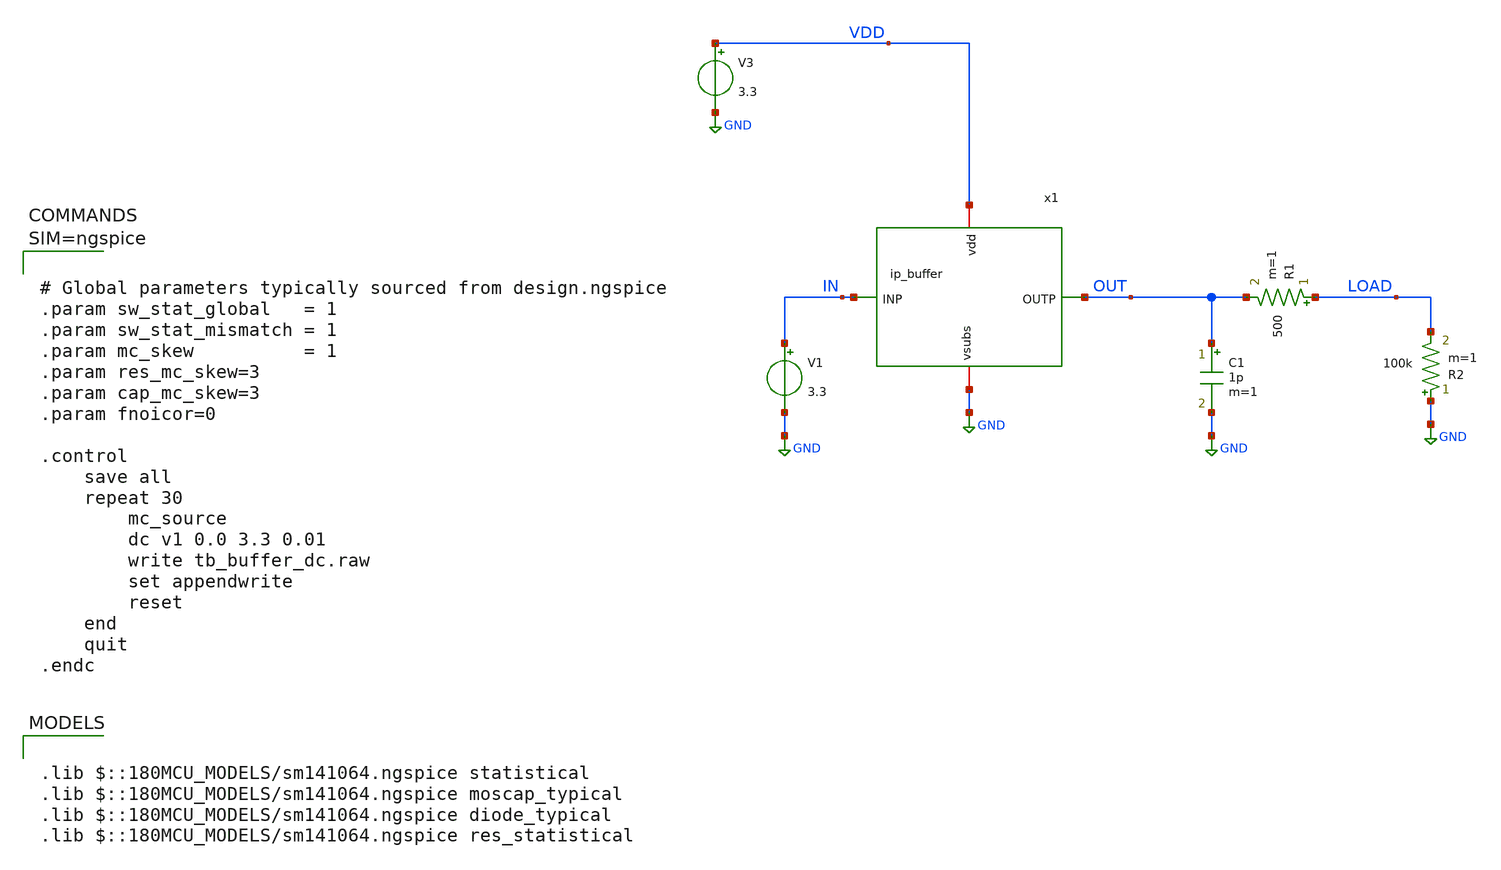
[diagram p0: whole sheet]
** sch_path: xschem/tb_buffer_dc.sch
**.subckt tb_buffer_dc
x1 VDD OUT IN GND ip_buffer
V3 VDD GND 3.3
V1 IN GND 3.3
R1 LOAD OUT 500 m=1
C1 OUT GND 1p m=1
R2 GND LOAD 100k m=1
**** begin user architecture code

.lib $::180MCU_MODELS/sm141064.ngspice statistical
.lib $::180MCU_MODELS/sm141064.ngspice moscap_typical
.lib $::180MCU_MODELS/sm141064.ngspice diode_typical
.lib $::180MCU_MODELS/sm141064.ngspice res_statistical




# Global parameters typically sourced from design.ngspice
.param sw_stat_global   = 1
.param sw_stat_mismatch = 1
.param mc_skew          = 1
.param res_mc_skew=3
.param cap_mc_skew=3
.param fnoicor=0

.control
	save all
	repeat 30
		mc_source
		dc v1 0.0 3.3 0.01
		write tb_buffer_dc.raw
		set appendwrite
		reset
	end
	quit
.endc



**** end user architecture code
**.ends

* expanding   symbol:  ip_buffer.sym # of pins=4
** sym_path: xschem/ip_buffer.sym
** sch_path: xschem/ip_buffer.sch
.subckt ip_buffer vdd OUTP INP vsubs
*.iopin vsubs
*.iopin vdd
*.ipin INP
*.opin OUTP
XM1 vsubs INP OUTP OUTP pfet_06v0 L=1u W=10u nf=1 ad='int((nf+1)/2) * W/nf * 0.18u' as='int((nf+2)/2) * W/nf * 0.18u'
+ pd='2*int((nf+1)/2) * (W/nf + 0.18u)' ps='2*int((nf+2)/2) * (W/nf + 0.18u)' nrd='0.18u / W' nrs='0.18u / W'
+ sa=0 sb=0 sd=0 m=15
Vmeas net1 net2 0
XM4 OUTP net1 vdd vdd pfet_06v0 L=2u W=10u nf=1 ad='int((nf+1)/2) * W/nf * 0.18u' as='int((nf+2)/2) * W/nf * 0.18u'
+ pd='2*int((nf+1)/2) * (W/nf + 0.18u)' ps='2*int((nf+2)/2) * (W/nf + 0.18u)' nrd='0.18u / W' nrs='0.18u / W'
+ sa=0 sb=0 sd=0 m=5
XM2 net1 net1 vdd vdd pfet_06v0 L=2u W=10u nf=1 ad='int((nf+1)/2) * W/nf * 0.18u' as='int((nf+2)/2) * W/nf * 0.18u'
+ pd='2*int((nf+1)/2) * (W/nf + 0.18u)' ps='2*int((nf+2)/2) * (W/nf + 0.18u)' nrd='0.18u / W' nrs='0.18u / W'
+ sa=0 sb=0 sd=0 m=4
XR1 net4 net2 vsubs ppolyf_u_1k_6p0 r_width=1e-6 r_length=6e-6 m=1
XR2 net3 net4 vsubs ppolyf_u_1k_6p0 r_width=1e-6 r_length=6e-6 m=1
XR3 net5 net3 vsubs ppolyf_u_1k_6p0 r_width=1e-6 r_length=6e-6 m=1
XR4 vsubs net5 vsubs ppolyf_u_1k_6p0 r_width=1e-6 r_length=6e-6 m=1
.ends

.GLOBAL GND
.end
